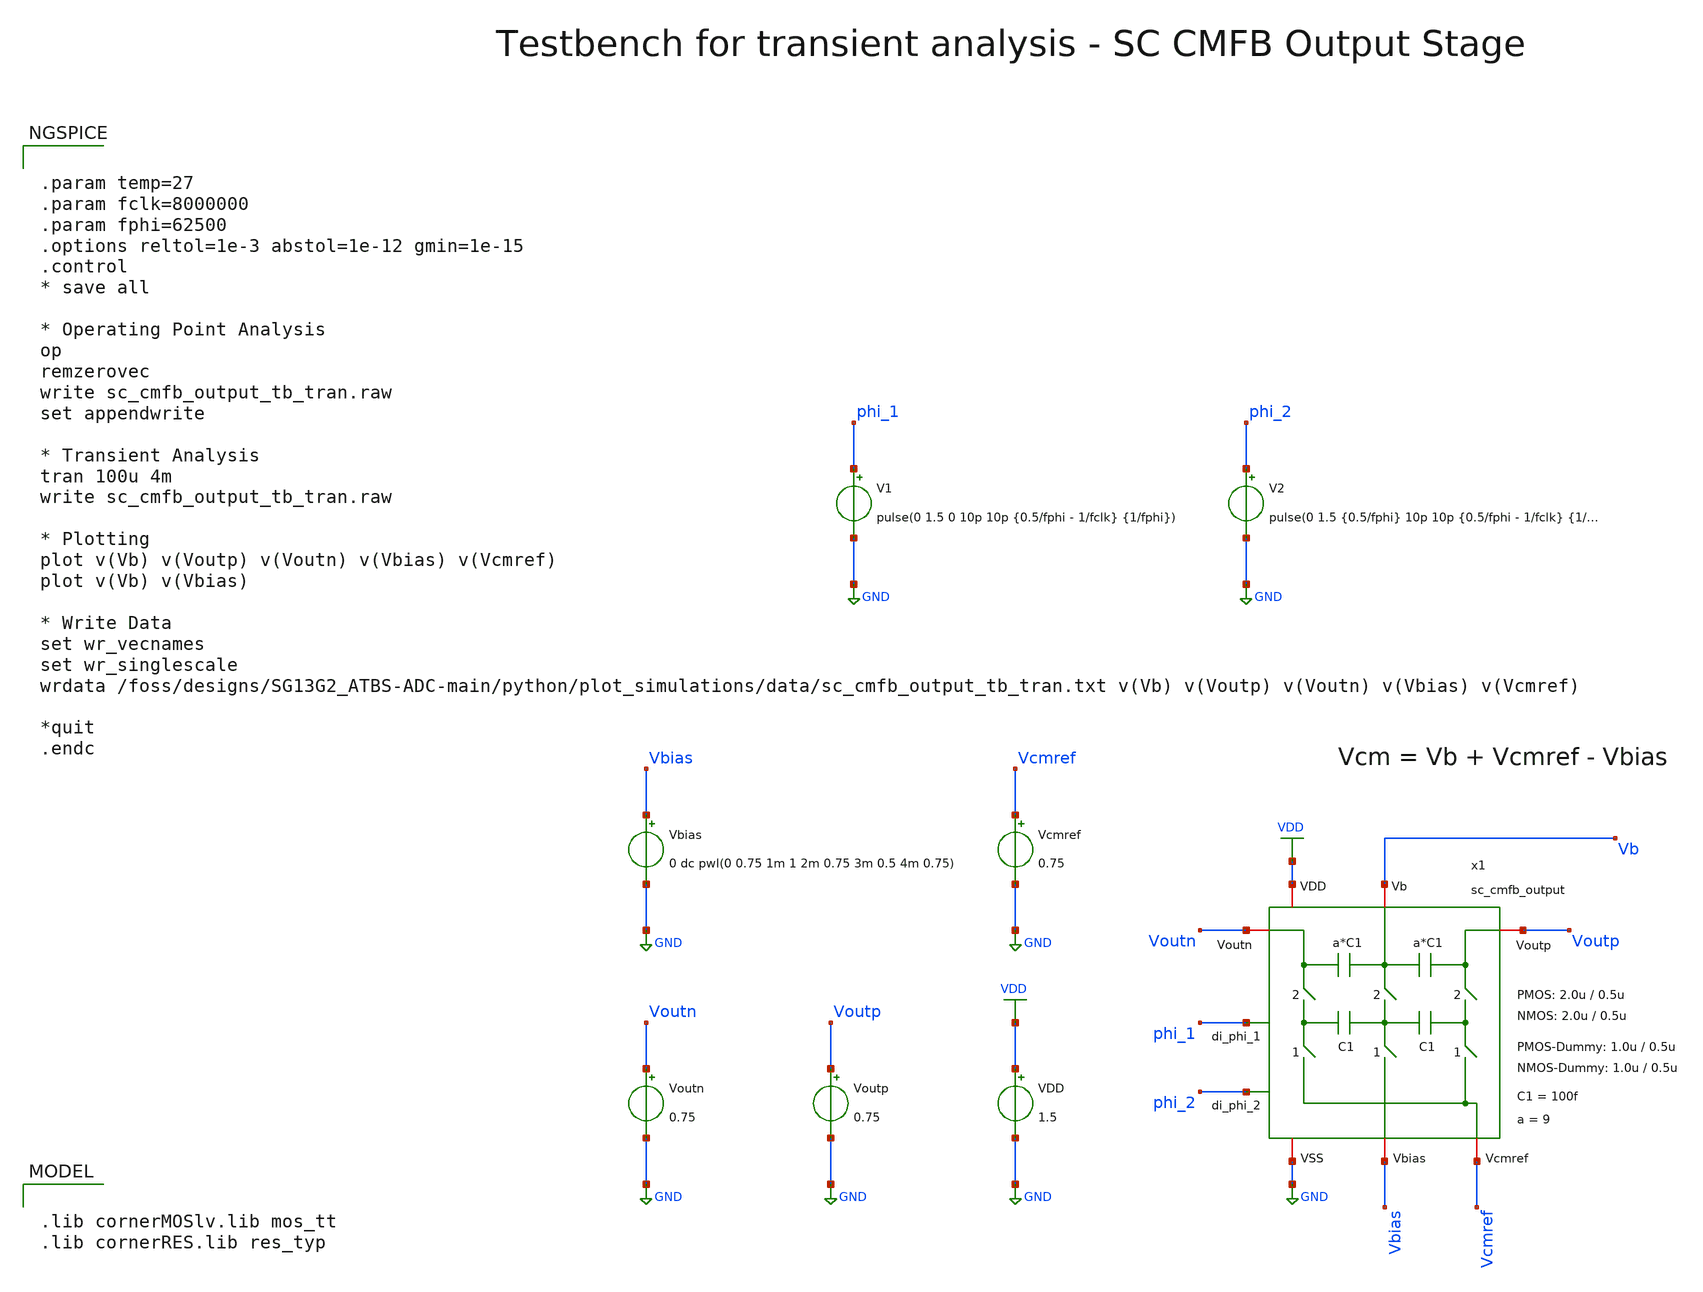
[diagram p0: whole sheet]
** sch_path: SG13G2_ATBS-ADC-main/xschem/bio_amplifier/amplifier_core/sc_cmfb/testbenches/sc_cmfb_output_tb_tran.sch
**.subckt sc_cmfb_output_tb_tran
VDD VDD GND 1.5
V1 phi_1 GND pulse(0 1.5 0 10p 10p {0.5/fphi - 1/fclk} {1/fphi})
V2 phi_2 GND pulse(0 1.5 {0.5/fphi} 10p 10p {0.5/fphi - 1/fclk} {1/fphi})
Voutn Voutn GND 0.75
Voutp Voutp GND 0.75
Vbias Vbias GND 0 dc pwl(0 0.75 1m 1 2m 0.75 3m 0.5 4m 0.75)
Vcmref Vcmref GND 0.75
x1 Vcmref Vbias phi_1 phi_2 VDD Voutp GND Vb Voutn sc_cmfb_output W_P_CMFB=2.0u L_P_CMFB=0.5u
+ W_N_CMFB=2.0u L_N_CMFB=0.5u W_P_CMFB_D=1.0u W_N_CMFB_D=1.0u C1=100f a=9
**** begin user architecture code

.lib cornerMOSlv.lib mos_tt
.lib cornerRES.lib res_typ



.param temp=27
.param fclk=8000000
.param fphi=62500
.options reltol=1e-3 abstol=1e-12 gmin=1e-15
.control
* save all

* Operating Point Analysis
op
remzerovec
write sc_cmfb_output_tb_tran.raw
set appendwrite

* Transient Analysis
tran 100u 4m
write sc_cmfb_output_tb_tran.raw

* Plotting
plot v(Vb) v(Voutp) v(Voutn) v(Vbias) v(Vcmref)
plot v(Vb) v(Vbias)

* Write Data
set wr_vecnames
set wr_singlescale
wrdata /foss/designs/SG13G2_ATBS-ADC-main/python/plot_simulations/data/sc_cmfb_output_tb_tran.txt
+ v(Vb) v(Voutp) v(Voutn) v(Vbias) v(Vcmref)

*quit
.endc

**** end user architecture code
**.ends

* expanding   symbol:  bio_amplifier/amplifier_core/sc_cmfb/sc_cmfb_output.sym # of pins=9
** sym_path: SG13G2_ATBS-ADC-main/xschem/bio_amplifier/amplifier_core/sc_cmfb/sc_cmfb_output.sym
** sch_path: SG13G2_ATBS-ADC-main/xschem/bio_amplifier/amplifier_core/sc_cmfb/sc_cmfb_output.sch
.subckt sc_cmfb_output Vcmref Vbias di_phi_1 di_phi_2 VDD Voutp VSS Vb Voutn  W_P_CMFB=2.0u
+ L_P_CMFB=0.5u W_N_CMFB=2.0u L_N_CMFB=0.5u W_P_CMFB_D=1.0u W_N_CMFB_D=1.0u C1=100f a=9
*.iopin VSS
*.iopin VDD
*.iopin Vb
*.iopin Voutp
*.iopin Voutn
*.iopin Vbias
*.iopin Vcmref
*.ipin di_phi_1
*.ipin di_phi_2
x1 VDD di_phi_2 VSS net1 Voutp di_phi_2_n transmission_gate_lv_wo_dummy W_P=W_P_CMFB L_P=L_P_CMFB
+ W_N=W_N_CMFB L_N=L_N_CMFB
C1 Voutp Vb {a*C1} m=1
x2 VDD di_phi_2 VSS net3 Vb di_phi_2_n transmission_gate_lv_wo_dummy W_P=W_P_CMFB L_P=L_P_CMFB
+ W_N=W_N_CMFB L_N=L_N_CMFB
x3 VDD di_phi_2 VSS net2 Voutn di_phi_2_n transmission_gate_lv_wo_dummy W_P=W_P_CMFB L_P=L_P_CMFB
+ W_N=W_N_CMFB L_N=L_N_CMFB
C2 Vb Voutn {a*C1} m=1
C3 net1 net3 C1 m=1
C4 net3 net2 C1 m=1
x7 VDD di_phi_1 di_phi_1_n VSS inverter_lv W_P=W_P_CMFB/2 L_P=L_P_CMFB W_N=W_N_CMFB/2 L_N=L_N_CMFB
x8 VDD di_phi_2 di_phi_2_n VSS inverter_lv W_P=W_P_CMFB/2 L_P=L_P_CMFB W_N=W_N_CMFB/2 L_N=L_N_CMFB
x4 VDD di_phi_1 VSS Vcmref net1 di_phi_1_n transmission_gate_lv_w_dummy W_P=W_P_CMFB L_P=L_P_CMFB
+ W_N=W_N_CMFB L_N=L_N_CMFB W_P_D=W_P_CMFB_D L_P_D=L_P_CMFB W_N_D=W_N_CMFB_D L_N_D=L_N_CMFB
x5 VDD di_phi_1 VSS Vbias net3 di_phi_1_n transmission_gate_lv_w_dummy W_P=W_P_CMFB L_P=L_P_CMFB
+ W_N=W_N_CMFB L_N=L_N_CMFB W_P_D=W_P_CMFB_D L_P_D=L_P_CMFB W_N_D=W_N_CMFB_D L_N_D=L_N_CMFB
x6 VDD di_phi_1 VSS Vcmref net2 di_phi_1_n transmission_gate_lv_w_dummy W_P=W_P_CMFB L_P=L_P_CMFB
+ W_N=W_N_CMFB L_N=L_N_CMFB W_P_D=W_P_CMFB_D L_P_D=L_P_CMFB W_N_D=W_N_CMFB_D L_N_D=L_N_CMFB
.ends


* expanding   symbol:  transmission_gate/transmission_gate_lv_wo_dummy.sym # of pins=6
** sym_path: SG13G2_ATBS-ADC-main/xschem/transmission_gate/transmission_gate_lv_wo_dummy.sym
** sch_path: SG13G2_ATBS-ADC-main/xschem/transmission_gate/transmission_gate_lv_wo_dummy.sch
.subckt transmission_gate_lv_wo_dummy VDD di_tg_ctrl VSS v_b v_a di_tg_ctrl_n  W_P=1.0u L_P=0.13u
+ W_N=1.0u L_N=0.13u
*.iopin v_a
*.iopin v_b
*.iopin VDD
*.iopin VSS
*.ipin di_tg_ctrl
*.ipin di_tg_ctrl_n
XM1 v_a di_tg_ctrl v_b VSS sg13_lv_nmos w=W_N l=L_N ng=1 m=1 mm_ok=1
XM2 v_a di_tg_ctrl_n v_b VDD sg13_lv_pmos w=W_P l=L_P ng=1 m=1 mm_ok=1
.ends


* expanding   symbol:  inverter/inverter_lv.sym # of pins=4
** sym_path: SG13G2_ATBS-ADC-main/xschem/inverter/inverter_lv.sym
** sch_path: SG13G2_ATBS-ADC-main/xschem/inverter/inverter_lv.sch
.subckt inverter_lv VDD vin vout VSS  W_P=3.0u L_P=0.13u W_N=1.0u L_N=0.13u
*.ipin vin
*.iopin VDD
*.iopin VSS
*.opin vout
XM1 vout vin VDD VDD sg13_lv_pmos w=W_P l=L_P ng=1 m=1 mm_ok=1
XM2 vout vin VSS VSS sg13_lv_nmos w=W_N l=L_N ng=1 m=1 mm_ok=1
.ends


* expanding   symbol:  transmission_gate/transmission_gate_lv_w_dummy.sym # of pins=6
** sym_path: SG13G2_ATBS-ADC-main/xschem/transmission_gate/transmission_gate_lv_w_dummy.sym
** sch_path: SG13G2_ATBS-ADC-main/xschem/transmission_gate/transmission_gate_lv_w_dummy.sch
.subckt transmission_gate_lv_w_dummy VDD di_tg_ctrl VSS v_b v_a di_tg_ctrl_n  W_P=2.0u L_P=0.13u
+ W_N=2.0u L_N=0.13u W_P_D=1.0u L_P_D=0.13u W_N_D=1.0u L_N_D=0.13u
*.iopin v_a
*.iopin v_b
*.iopin VDD
*.iopin VSS
*.ipin di_tg_ctrl
*.ipin di_tg_ctrl_n
XM1 v_a di_tg_ctrl v_b VSS sg13_lv_nmos w=W_N l=L_N ng=1 m=1 mm_ok=1
XM2 v_a di_tg_ctrl_n v_b VDD sg13_lv_pmos w=W_P l=L_P ng=1 m=1 mm_ok=1
XMdummy2 v_b di_tg_ctrl v_b VDD sg13_lv_pmos w=W_P_D l=L_P_D ng=1 m=1 mm_ok=1
XMdummy1 v_b di_tg_ctrl_n v_b VSS sg13_lv_nmos w=W_N_D l=L_N_D ng=1 m=1 mm_ok=1
.ends

.GLOBAL GND
.GLOBAL VDD
.end
